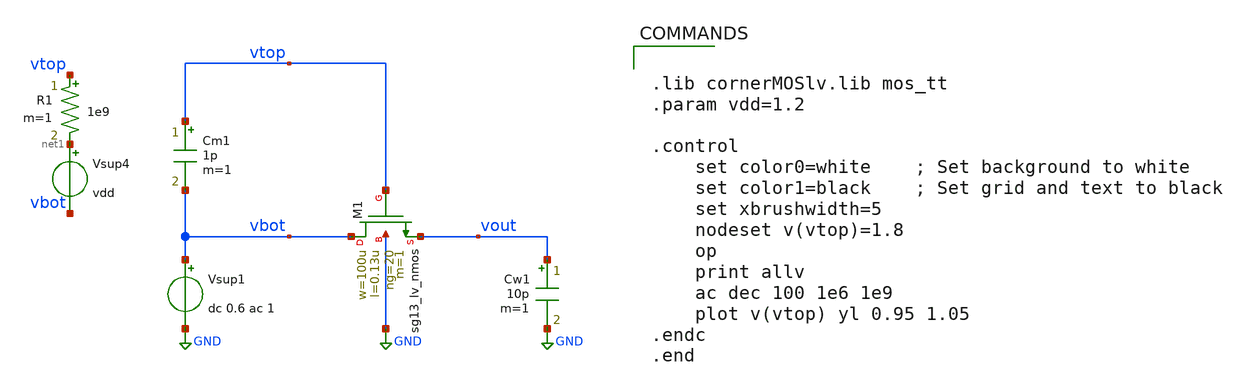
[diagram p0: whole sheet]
** sch_path: xschem/tb_csmall.sch
**.subckt tb_csmall
Cw1 vout GND 10p m=1
Vsup1 vbot GND dc 0.6 ac 1
Cm1 vtop vbot 1p m=1
XM1 vbot vtop vout GND sg13_lv_nmos w=100u l=0.13u ng=20 m=1 mm_ok=1
Vsup4 net1 vbot vdd
R1 vtop net1 1e9 m=1
**** begin user architecture code


.lib cornerMOSlv.lib mos_tt
.param vdd=1.2

.control
    set color0=white    ; Set background to white
    set color1=black    ; Set grid and text to black
    set xbrushwidth=5
    nodeset v(vtop)=1.8
    op
    print allv
    ac dec 100 1e6 1e9
    plot v(vtop) yl 0.95 1.05
.endc
.end


**** end user architecture code
**.ends
.GLOBAL GND
.end
